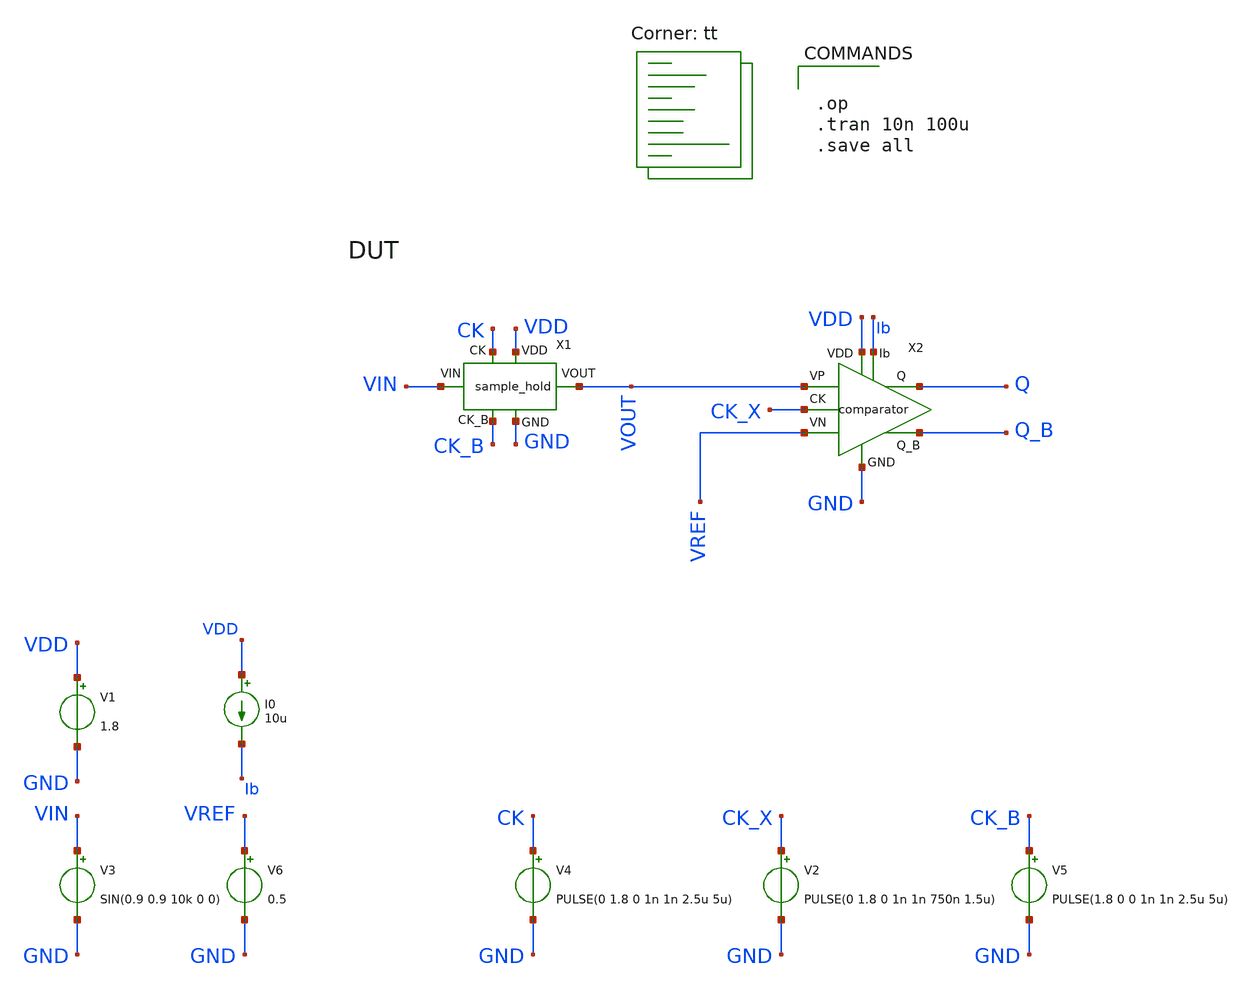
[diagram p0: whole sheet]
** sch_path: xschem/adc_top.sch
**.subckt adc_top
X1 GND VDD VIN VOUT CK CK_B sample_hold
V1 VDD GND 1.8
V3 VIN GND SIN(0.9 0.9 10k 0 0)
V4 CK GND PULSE(0 1.8 0 1n 1n 2.5u 5u)
V5 CK_B GND PULSE(1.8 0 0 1n 1n 2.5u 5u)
V2 CK_X GND PULSE(0 1.8 0 1n 1n 750n 1.5u)
V6 VREF GND 0.5
X2 VOUT VREF GND Q_B Q VDD CK_X Ib comparator
I0 VDD Ib 10u
**** begin user architecture code
.lib $::SKYWATER_MODELS/sky130.lib.spice tt


.op
.tran 10n 100u
.save all


**** end user architecture code
**.ends
.end
